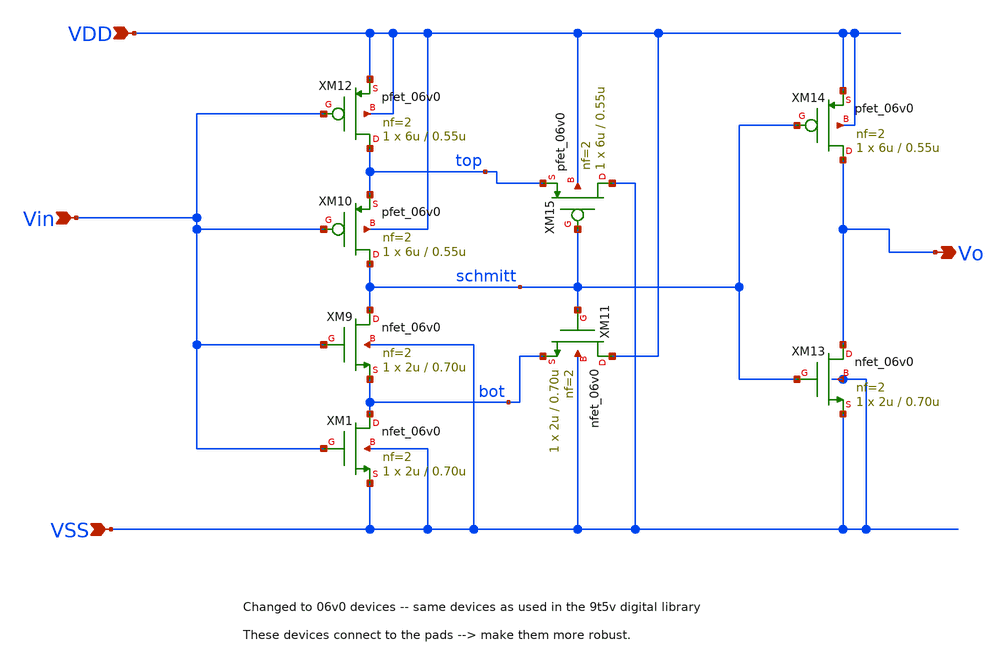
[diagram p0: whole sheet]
** sch_path: Schmitt/Schmitt.sch
**.subckt Schmitt VDD VSS Vin Vo
*.ipin VDD
*.ipin VSS
*.ipin Vin
*.opin Vo
XM9 schmitt Vin bot VSS nfet_06v0 L=0.70u W=2u nf=2 ad='int((nf+1)/2) * W/nf * 0.18u' as='int((nf+2)/2) * W/nf * 0.18u'
+ pd='2*int((nf+1)/2) * (W/nf + 0.18u)' ps='2*int((nf+2)/2) * (W/nf + 0.18u)' nrd='0.18u / W' nrs='0.18u / W'
+ sa=0 sb=0 sd=0 m=1
XM10 schmitt Vin top VDD pfet_06v0 L=0.55u W=6u nf=2 ad='int((nf+1)/2) * W/nf * 0.18u' as='int((nf+2)/2) * W/nf * 0.18u'
+ pd='2*int((nf+1)/2) * (W/nf + 0.18u)' ps='2*int((nf+2)/2) * (W/nf + 0.18u)' nrd='0.18u / W' nrs='0.18u / W'
+ sa=0 sb=0 sd=0 m=1
XM11 VDD schmitt bot VSS nfet_06v0 L=0.70u W=2u nf=2 ad='int((nf+1)/2) * W/nf * 0.18u' as='int((nf+2)/2) * W/nf * 0.18u'
+ pd='2*int((nf+1)/2) * (W/nf + 0.18u)' ps='2*int((nf+2)/2) * (W/nf + 0.18u)' nrd='0.18u / W' nrs='0.18u / W'
+ sa=0 sb=0 sd=0 m=1
XM12 top Vin VDD VDD pfet_06v0 L=0.55u W=6u nf=2 ad='int((nf+1)/2) * W/nf * 0.18u' as='int((nf+2)/2) * W/nf * 0.18u'
+ pd='2*int((nf+1)/2) * (W/nf + 0.18u)' ps='2*int((nf+2)/2) * (W/nf + 0.18u)' nrd='0.18u / W' nrs='0.18u / W'
+ sa=0 sb=0 sd=0 m=1
XM13 Vo schmitt VSS VSS nfet_06v0 L=0.70u W=2u nf=2 ad='int((nf+1)/2) * W/nf * 0.18u' as='int((nf+2)/2) * W/nf * 0.18u'
+ pd='2*int((nf+1)/2) * (W/nf + 0.18u)' ps='2*int((nf+2)/2) * (W/nf + 0.18u)' nrd='0.18u / W' nrs='0.18u / W'
+ sa=0 sb=0 sd=0 m=1
XM14 Vo schmitt VDD VDD pfet_06v0 L=0.55u W=6u nf=2 ad='int((nf+1)/2) * W/nf * 0.18u' as='int((nf+2)/2) * W/nf * 0.18u'
+ pd='2*int((nf+1)/2) * (W/nf + 0.18u)' ps='2*int((nf+2)/2) * (W/nf + 0.18u)' nrd='0.18u / W' nrs='0.18u / W'
+ sa=0 sb=0 sd=0 m=1
XM15 VSS schmitt top VDD pfet_06v0 L=0.55u W=6u nf=2 ad='int((nf+1)/2) * W/nf * 0.18u' as='int((nf+2)/2) * W/nf * 0.18u'
+ pd='2*int((nf+1)/2) * (W/nf + 0.18u)' ps='2*int((nf+2)/2) * (W/nf + 0.18u)' nrd='0.18u / W' nrs='0.18u / W'
+ sa=0 sb=0 sd=0 m=1
XM1 bot Vin VSS VSS nfet_06v0 L=0.70u W=2u nf=2 ad='int((nf+1)/2) * W/nf * 0.18u' as='int((nf+2)/2) * W/nf * 0.18u'
+ pd='2*int((nf+1)/2) * (W/nf + 0.18u)' ps='2*int((nf+2)/2) * (W/nf + 0.18u)' nrd='0.18u / W' nrs='0.18u / W'
+ sa=0 sb=0 sd=0 m=1
**.ends
.end
